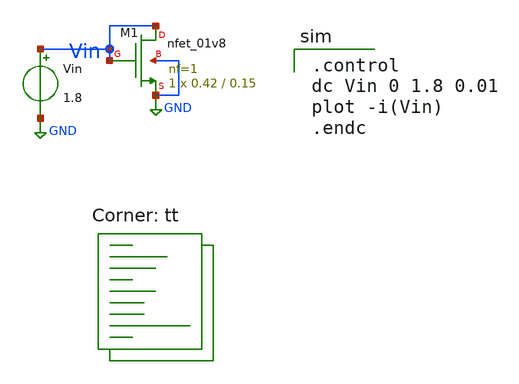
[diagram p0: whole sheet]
** sch_path: tutorial_2/tutorial_2_1a (copy 1).sch
**.subckt tutorial_2_1a (copy 1)
XM1 Vin Vin GND GND sky130_fd_pr__nfet_01v8 L=0.15 W=0.42 nf=1 ad='int((nf+1)/2) * W/nf * 0.29' as='int((nf+2)/2) * W/nf * 0.29'
+ pd='2*int((nf+1)/2) * (W/nf + 0.29)' ps='2*int((nf+2)/2) * (W/nf + 0.29)' nrd='0.29 / W' nrs='0.29 / W'
+ sa=0 sb=0 sd=0 mult=1 m=1
Vin Vin GND 1.8
**** begin user architecture code

.control
dc Vin 0 1.8 0.01
plot -i(Vin)
.endc

.lib $::SKYWATER_MODELS/sky130.lib.spice tt
**** end user architecture code
**.ends
.GLOBAL GND
.end
